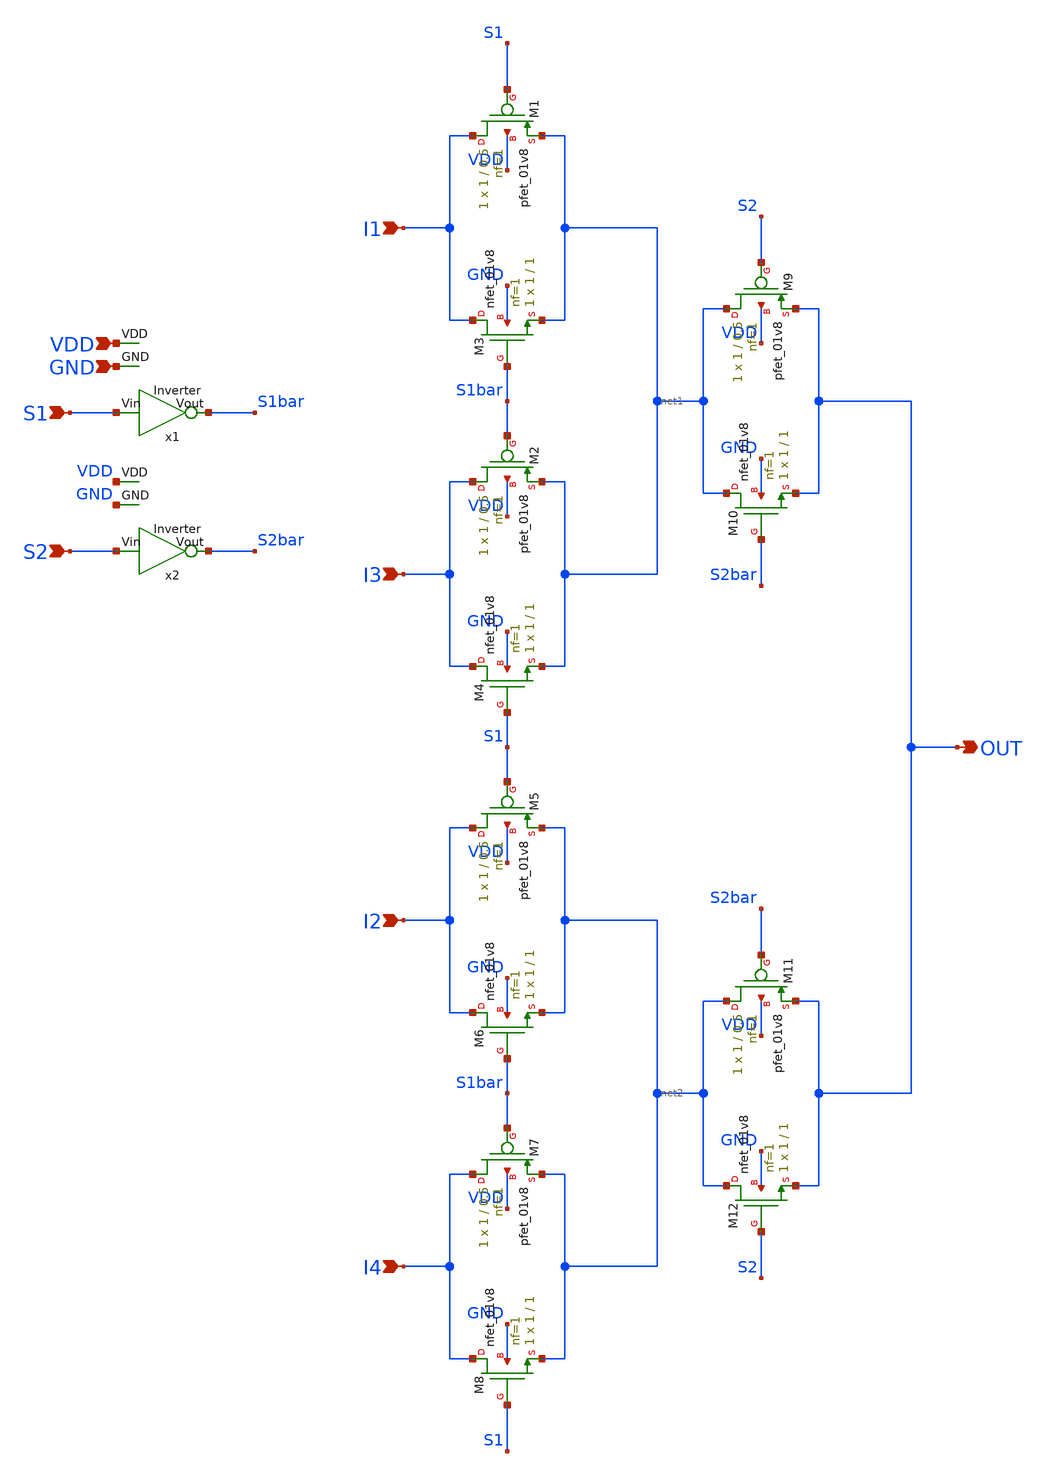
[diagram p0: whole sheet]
** sch_path: xschem/4-to-1_analog_MUX.sch
**.subckt 4-to-1_analog_MUX I1 I2 I3 I4 OUT S1 S2 VDD GND
*.ipin I1
*.ipin I2
*.ipin I3
*.ipin I4
*.opin OUT
*.ipin S1
*.ipin S2
*.ipin VDD
*.ipin GND
x1 S1 S1bar GND VDD Inverter
x2 S2 S2bar GND VDD Inverter
XM9 net1 S2 OUT VDD sky130_fd_pr__pfet_01v8 L=0.5 W=1 nf=1 ad='int((nf+1)/2) * W/nf * 0.29' as='int((nf+2)/2) * W/nf * 0.29'
+ pd='2*int((nf+1)/2) * (W/nf + 0.29)' ps='2*int((nf+2)/2) * (W/nf + 0.29)' nrd='0.29 / W' nrs='0.29 / W'
+ sa=0 sb=0 sd=0 mult=1 m=1
XM1 I1 S1 net1 VDD sky130_fd_pr__pfet_01v8 L=0.5 W=1 nf=1 ad='int((nf+1)/2) * W/nf * 0.29' as='int((nf+2)/2) * W/nf * 0.29'
+ pd='2*int((nf+1)/2) * (W/nf + 0.29)' ps='2*int((nf+2)/2) * (W/nf + 0.29)' nrd='0.29 / W' nrs='0.29 / W'
+ sa=0 sb=0 sd=0 mult=1 m=1
XM2 I3 S1bar net1 VDD sky130_fd_pr__pfet_01v8 L=0.5 W=1 nf=1 ad='int((nf+1)/2) * W/nf * 0.29' as='int((nf+2)/2) * W/nf * 0.29'
+ pd='2*int((nf+1)/2) * (W/nf + 0.29)' ps='2*int((nf+2)/2) * (W/nf + 0.29)' nrd='0.29 / W' nrs='0.29 / W'
+ sa=0 sb=0 sd=0 mult=1 m=1
XM5 I2 S1 net2 VDD sky130_fd_pr__pfet_01v8 L=0.5 W=1 nf=1 ad='int((nf+1)/2) * W/nf * 0.29' as='int((nf+2)/2) * W/nf * 0.29'
+ pd='2*int((nf+1)/2) * (W/nf + 0.29)' ps='2*int((nf+2)/2) * (W/nf + 0.29)' nrd='0.29 / W' nrs='0.29 / W'
+ sa=0 sb=0 sd=0 mult=1 m=1
XM7 I4 S1bar net2 VDD sky130_fd_pr__pfet_01v8 L=0.5 W=1 nf=1 ad='int((nf+1)/2) * W/nf * 0.29' as='int((nf+2)/2) * W/nf * 0.29'
+ pd='2*int((nf+1)/2) * (W/nf + 0.29)' ps='2*int((nf+2)/2) * (W/nf + 0.29)' nrd='0.29 / W' nrs='0.29 / W'
+ sa=0 sb=0 sd=0 mult=1 m=1
XM11 net2 S2bar OUT VDD sky130_fd_pr__pfet_01v8 L=0.5 W=1 nf=1 ad='int((nf+1)/2) * W/nf * 0.29' as='int((nf+2)/2) * W/nf * 0.29'
+ pd='2*int((nf+1)/2) * (W/nf + 0.29)' ps='2*int((nf+2)/2) * (W/nf + 0.29)' nrd='0.29 / W' nrs='0.29 / W'
+ sa=0 sb=0 sd=0 mult=1 m=1
XM3 I1 S1bar net1 GND sky130_fd_pr__nfet_01v8 L=1 W=1 nf=1 ad='int((nf+1)/2) * W/nf * 0.29' as='int((nf+2)/2) * W/nf * 0.29'
+ pd='2*int((nf+1)/2) * (W/nf + 0.29)' ps='2*int((nf+2)/2) * (W/nf + 0.29)' nrd='0.29 / W' nrs='0.29 / W'
+ sa=0 sb=0 sd=0 mult=1 m=1
XM4 I3 S1 net1 GND sky130_fd_pr__nfet_01v8 L=1 W=1 nf=1 ad='int((nf+1)/2) * W/nf * 0.29' as='int((nf+2)/2) * W/nf * 0.29'
+ pd='2*int((nf+1)/2) * (W/nf + 0.29)' ps='2*int((nf+2)/2) * (W/nf + 0.29)' nrd='0.29 / W' nrs='0.29 / W'
+ sa=0 sb=0 sd=0 mult=1 m=1
XM10 net1 S2bar OUT GND sky130_fd_pr__nfet_01v8 L=1 W=1 nf=1 ad='int((nf+1)/2) * W/nf * 0.29' as='int((nf+2)/2) * W/nf * 0.29'
+ pd='2*int((nf+1)/2) * (W/nf + 0.29)' ps='2*int((nf+2)/2) * (W/nf + 0.29)' nrd='0.29 / W' nrs='0.29 / W'
+ sa=0 sb=0 sd=0 mult=1 m=1
XM6 I2 S1bar net2 GND sky130_fd_pr__nfet_01v8 L=1 W=1 nf=1 ad='int((nf+1)/2) * W/nf * 0.29' as='int((nf+2)/2) * W/nf * 0.29'
+ pd='2*int((nf+1)/2) * (W/nf + 0.29)' ps='2*int((nf+2)/2) * (W/nf + 0.29)' nrd='0.29 / W' nrs='0.29 / W'
+ sa=0 sb=0 sd=0 mult=1 m=1
XM8 I4 S1 net2 GND sky130_fd_pr__nfet_01v8 L=1 W=1 nf=1 ad='int((nf+1)/2) * W/nf * 0.29' as='int((nf+2)/2) * W/nf * 0.29'
+ pd='2*int((nf+1)/2) * (W/nf + 0.29)' ps='2*int((nf+2)/2) * (W/nf + 0.29)' nrd='0.29 / W' nrs='0.29 / W'
+ sa=0 sb=0 sd=0 mult=1 m=1
XM12 net2 S2 OUT GND sky130_fd_pr__nfet_01v8 L=1 W=1 nf=1 ad='int((nf+1)/2) * W/nf * 0.29' as='int((nf+2)/2) * W/nf * 0.29'
+ pd='2*int((nf+1)/2) * (W/nf + 0.29)' ps='2*int((nf+2)/2) * (W/nf + 0.29)' nrd='0.29 / W' nrs='0.29 / W'
+ sa=0 sb=0 sd=0 mult=1 m=1
**.ends

* expanding   symbol:  Inverter.sym # of pins=4
** sym_path: xschem/Inverter.sym
** sch_path: xschem/Inverter.sch
.subckt Inverter Vin Vout GND VDD
*.opin Vout
*.ipin Vin
*.ipin VDD
*.ipin GND
XM1 Vout Vin VDD VDD sky130_fd_pr__pfet_01v8 L=0.5 W=1 nf=1 ad='int((nf+1)/2) * W/nf * 0.29' as='int((nf+2)/2) * W/nf * 0.29'
+ pd='2*int((nf+1)/2) * (W/nf + 0.29)' ps='2*int((nf+2)/2) * (W/nf + 0.29)' nrd='0.29 / W' nrs='0.29 / W'
+ sa=0 sb=0 sd=0 mult=1 m=1
XM2 Vout Vin GND GND sky130_fd_pr__nfet_01v8 L=1 W=1 nf=1 ad='int((nf+1)/2) * W/nf * 0.29' as='int((nf+2)/2) * W/nf * 0.29'
+ pd='2*int((nf+1)/2) * (W/nf + 0.29)' ps='2*int((nf+2)/2) * (W/nf + 0.29)' nrd='0.29 / W' nrs='0.29 / W'
+ sa=0 sb=0 sd=0 mult=1 m=1
.ends

.end
